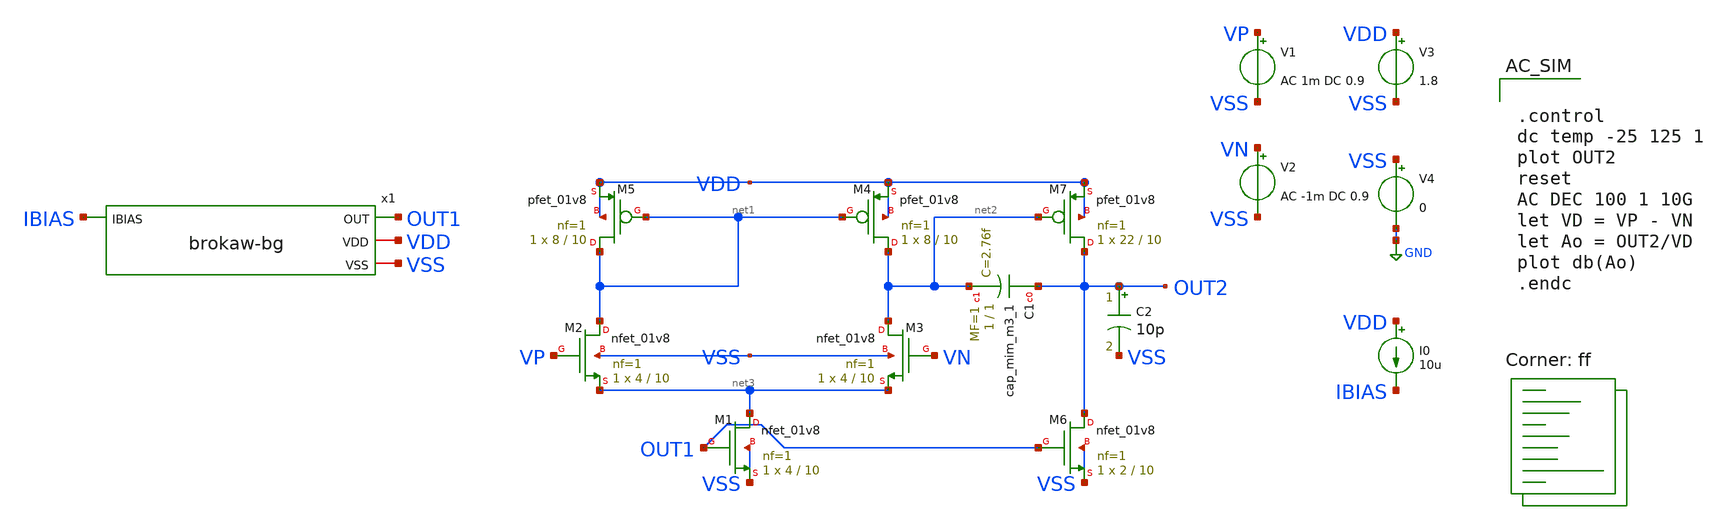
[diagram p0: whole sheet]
** sch_path: designs/libs/core_analog/core_bandgap/brokaw-bandgap/tb_bg-ota.sch
**.subckt tb_bg-ota
XM1 net3 OUT1 VSS VSS sky130_fd_pr__nfet_01v8 L=10 W=4 nf=1 ad='int((nf+1)/2) * W/nf * 0.29' as='int((nf+2)/2) * W/nf * 0.29'
+ pd='2*int((nf+1)/2) * (W/nf + 0.29)' ps='2*int((nf+2)/2) * (W/nf + 0.29)' nrd='0.29 / W' nrs='0.29 / W'
+ sa=0 sb=0 sd=0 mult=1 m=1
XM2 net1 VP net3 VSS sky130_fd_pr__nfet_01v8 L=10 W=4 nf=1 ad='int((nf+1)/2) * W/nf * 0.29' as='int((nf+2)/2) * W/nf * 0.29'
+ pd='2*int((nf+1)/2) * (W/nf + 0.29)' ps='2*int((nf+2)/2) * (W/nf + 0.29)' nrd='0.29 / W' nrs='0.29 / W'
+ sa=0 sb=0 sd=0 mult=1 m=1
XM3 net2 VN net3 VSS sky130_fd_pr__nfet_01v8 L=10 W=4 nf=1 ad='int((nf+1)/2) * W/nf * 0.29' as='int((nf+2)/2) * W/nf * 0.29'
+ pd='2*int((nf+1)/2) * (W/nf + 0.29)' ps='2*int((nf+2)/2) * (W/nf + 0.29)' nrd='0.29 / W' nrs='0.29 / W'
+ sa=0 sb=0 sd=0 mult=1 m=1
XM4 net2 net1 VDD VDD sky130_fd_pr__pfet_01v8 L=10 W=8 nf=1 ad='int((nf+1)/2) * W/nf * 0.29' as='int((nf+2)/2) * W/nf * 0.29'
+ pd='2*int((nf+1)/2) * (W/nf + 0.29)' ps='2*int((nf+2)/2) * (W/nf + 0.29)' nrd='0.29 / W' nrs='0.29 / W'
+ sa=0 sb=0 sd=0 mult=1 m=1
XM5 net1 net1 VDD VDD sky130_fd_pr__pfet_01v8 L=10 W=8 nf=1 ad='int((nf+1)/2) * W/nf * 0.29' as='int((nf+2)/2) * W/nf * 0.29'
+ pd='2*int((nf+1)/2) * (W/nf + 0.29)' ps='2*int((nf+2)/2) * (W/nf + 0.29)' nrd='0.29 / W' nrs='0.29 / W'
+ sa=0 sb=0 sd=0 mult=1 m=1
V3 VDD VSS 1.8
V4 VSS GND 0
I0 VDD IBIAS 10u
V1 VP VSS AC 1m DC 0.9
V2 VN VSS AC -1m DC 0.9
x1 IBIAS OUT1 VDD VSS brokaw-bg
XM6 OUT2 OUT1 VSS VSS sky130_fd_pr__nfet_01v8 L=10 W=2 nf=1 ad='int((nf+1)/2) * W/nf * 0.29' as='int((nf+2)/2) * W/nf * 0.29'
+ pd='2*int((nf+1)/2) * (W/nf + 0.29)' ps='2*int((nf+2)/2) * (W/nf + 0.29)' nrd='0.29 / W' nrs='0.29 / W'
+ sa=0 sb=0 sd=0 mult=1 m=1
XM7 OUT2 net2 VDD VDD sky130_fd_pr__pfet_01v8 L=10 W=22 nf=1 ad='int((nf+1)/2) * W/nf * 0.29' as='int((nf+2)/2) * W/nf * 0.29'
+ pd='2*int((nf+1)/2) * (W/nf + 0.29)' ps='2*int((nf+2)/2) * (W/nf + 0.29)' nrd='0.29 / W' nrs='0.29 / W'
+ sa=0 sb=0 sd=0 mult=1 m=1
XC1 OUT2 net2 sky130_fd_pr__cap_mim_m3_1 W=1 L=1 MF=1 m=1
C2 OUT2 VSS 10p m=1
**** begin user architecture code
.lib $::SKYWATER_MODELS/sky130.lib.spice ff


.control
dc temp -25 125 1
plot OUT2
reset
AC DEC 100 1 10G
let VD = VP - VN
let Ao = OUT2/VD
plot db(Ao)
.endc


**** end user architecture code
**.ends

* expanding   symbol:
*+  bandgap-referenced-ota/designs/libs/core_analog/core_bandgap/brokaw-bandgap/brokaw-bg.sym # of pins=4
** sym_path: designs/libs/core_analog/core_bandgap/brokaw-bandgap/brokaw-bg.sym
** sch_path: designs/libs/core_analog/core_bandgap/brokaw-bandgap/brokaw-bg.sch
.subckt brokaw-bg IBIAS OUT VDD VSS
*.iopin VDD
*.iopin VSS
*.opin OUT
*.ipin IBIAS
XR1 net1 VDD VSS sky130_fd_pr__res_xhigh_po W=1 L=1.25 mult=1 m=1
XR2 net2 VDD VSS sky130_fd_pr__res_xhigh_po W=1 L=1.25 mult=1 m=1
XQ1 net1 OUT net3 VSS sky130_fd_pr__npn_05v5_w1p00l2p00
XQ2 net2 OUT net4 VSS sky130_fd_pr__npn_05v5_w1p00l2p00
x1 net1 OUT IBIAS VSS net2 VDD n-ota-bg
XR3 net4 net3 VSS sky130_fd_pr__res_xhigh_po W=1 L=2 mult=1 m=1
XR4 VSS net4 VSS sky130_fd_pr__res_xhigh_po W=19 L=1 mult=1 m=1
.ends


* expanding   symbol:
*+  bandgap-referenced-ota/designs/libs/core_analog/core_bandgap/5t-ota/n-ota-bg.sym # of pins=6
** sym_path: designs/libs/core_analog/core_bandgap/5t-ota/n-ota-bg.sym
** sch_path: designs/libs/core_analog/core_bandgap/5t-ota/n-ota-bg.sch
.subckt n-ota-bg VN OUT IBIAS VSS VP VDD
*.iopin VDD
*.iopin VSS
*.ipin IBIAS
*.ipin VP
*.ipin VN
*.opin OUT
XM1 net2 VP net1 VSS sky130_fd_pr__nfet_01v8 L=4 W=4 nf=1 ad='int((nf+1)/2) * W/nf * 0.29' as='int((nf+2)/2) * W/nf * 0.29'
+ pd='2*int((nf+1)/2) * (W/nf + 0.29)' ps='2*int((nf+2)/2) * (W/nf + 0.29)' nrd='0.29 / W' nrs='0.29 / W'
+ sa=0 sb=0 sd=0 mult=1 m=1
XM2 net3 VN net1 VSS sky130_fd_pr__nfet_01v8 L=4 W=4 nf=1 ad='int((nf+1)/2) * W/nf * 0.29' as='int((nf+2)/2) * W/nf * 0.29'
+ pd='2*int((nf+1)/2) * (W/nf + 0.29)' ps='2*int((nf+2)/2) * (W/nf + 0.29)' nrd='0.29 / W' nrs='0.29 / W'
+ sa=0 sb=0 sd=0 mult=1 m=1
XM3 net1 IBIAS VSS VSS sky130_fd_pr__nfet_01v8 L=4 W=4 nf=1 ad='int((nf+1)/2) * W/nf * 0.29' as='int((nf+2)/2) * W/nf * 0.29'
+ pd='2*int((nf+1)/2) * (W/nf + 0.29)' ps='2*int((nf+2)/2) * (W/nf + 0.29)' nrd='0.29 / W' nrs='0.29 / W'
+ sa=0 sb=0 sd=0 mult=1 m=1
XM4 net3 net2 VDD VDD sky130_fd_pr__pfet_01v8 L=4 W=8 nf=1 ad='int((nf+1)/2) * W/nf * 0.29' as='int((nf+2)/2) * W/nf * 0.29'
+ pd='2*int((nf+1)/2) * (W/nf + 0.29)' ps='2*int((nf+2)/2) * (W/nf + 0.29)' nrd='0.29 / W' nrs='0.29 / W'
+ sa=0 sb=0 sd=0 mult=1 m=1
XM5 net2 net2 VDD VDD sky130_fd_pr__pfet_01v8 L=4 W=8 nf=1 ad='int((nf+1)/2) * W/nf * 0.29' as='int((nf+2)/2) * W/nf * 0.29'
+ pd='2*int((nf+1)/2) * (W/nf + 0.29)' ps='2*int((nf+2)/2) * (W/nf + 0.29)' nrd='0.29 / W' nrs='0.29 / W'
+ sa=0 sb=0 sd=0 mult=1 m=1
XM6 IBIAS IBIAS VSS VSS sky130_fd_pr__nfet_01v8 L=4 W=4 nf=1 ad='int((nf+1)/2) * W/nf * 0.29' as='int((nf+2)/2) * W/nf * 0.29'
+ pd='2*int((nf+1)/2) * (W/nf + 0.29)' ps='2*int((nf+2)/2) * (W/nf + 0.29)' nrd='0.29 / W' nrs='0.29 / W'
+ sa=0 sb=0 sd=0 mult=1 m=1
XM7 net3 net2 VDD VDD sky130_fd_pr__pfet_01v8 L=4 W=8 nf=1 ad='int((nf+1)/2) * W/nf * 0.29' as='int((nf+2)/2) * W/nf * 0.29'
+ pd='2*int((nf+1)/2) * (W/nf + 0.29)' ps='2*int((nf+2)/2) * (W/nf + 0.29)' nrd='0.29 / W' nrs='0.29 / W'
+ sa=0 sb=0 sd=0 mult=1 m=1
XM8 net2 net2 VDD VDD sky130_fd_pr__pfet_01v8 L=4 W=8 nf=1 ad='int((nf+1)/2) * W/nf * 0.29' as='int((nf+2)/2) * W/nf * 0.29'
+ pd='2*int((nf+1)/2) * (W/nf + 0.29)' ps='2*int((nf+2)/2) * (W/nf + 0.29)' nrd='0.29 / W' nrs='0.29 / W'
+ sa=0 sb=0 sd=0 mult=1 m=1
XM9 OUT net3 VDD VDD sky130_fd_pr__pfet_01v8 L=2 W=18 nf=1 ad='int((nf+1)/2) * W/nf * 0.29' as='int((nf+2)/2) * W/nf * 0.29'
+ pd='2*int((nf+1)/2) * (W/nf + 0.29)' ps='2*int((nf+2)/2) * (W/nf + 0.29)' nrd='0.29 / W' nrs='0.29 / W'
+ sa=0 sb=0 sd=0 mult=1 m=1
XM10 OUT IBIAS VSS VSS sky130_fd_pr__nfet_01v8 L=2 W=2 nf=1 ad='int((nf+1)/2) * W/nf * 0.29' as='int((nf+2)/2) * W/nf * 0.29'
+ pd='2*int((nf+1)/2) * (W/nf + 0.29)' ps='2*int((nf+2)/2) * (W/nf + 0.29)' nrd='0.29 / W' nrs='0.29 / W'
+ sa=0 sb=0 sd=0 mult=1 m=1
XC1 OUT net3 sky130_fd_pr__cap_mim_m3_1 W=25 L=1 MF=1 m=1
.ends

.GLOBAL GND
.end
